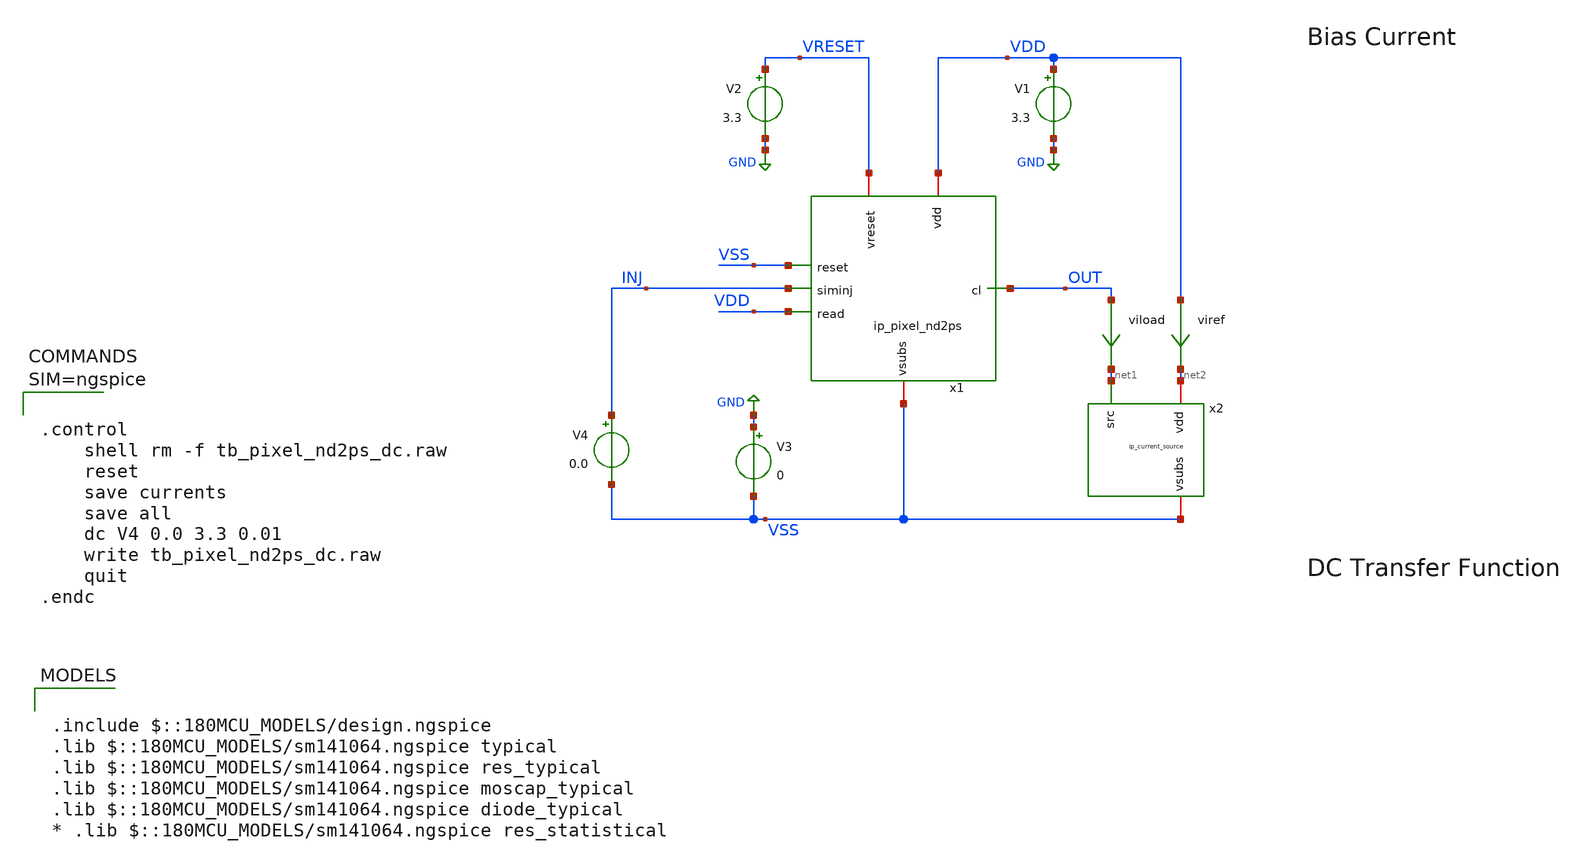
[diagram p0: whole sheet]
** sch_path: xschem/tb_pixel_nd2ps_dc.sch
**.subckt tb_pixel_nd2ps_dc
V1 VDD GND 3.3
V2 VRESET GND 3.3
V3 GND VSS 0
x1 VDD VRESET VSS INJ OUT VDD VSS ip_pixel_nd2ps
V4 INJ VSS 0.0
x2 net2 net1 VSS ip_current_source
viload OUT net1 0
.save i(viload)
viref VDD net2 0
.save i(viref)
**** begin user architecture code

.include $::180MCU_MODELS/design.ngspice
.lib $::180MCU_MODELS/sm141064.ngspice typical
.lib $::180MCU_MODELS/sm141064.ngspice res_typical
.lib $::180MCU_MODELS/sm141064.ngspice moscap_typical
.lib $::180MCU_MODELS/sm141064.ngspice diode_typical
* .lib $::180MCU_MODELS/sm141064.ngspice res_statistical




.control
	shell rm -f tb_pixel_nd2ps_dc.raw
	reset
	save currents
	save all
	dc V4 0.0 3.3 0.01
	write tb_pixel_nd2ps_dc.raw
	quit
.endc



**** end user architecture code
**.ends

* expanding   symbol:  ip_pixel_nd2ps.sym # of pins=7
** sym_path: xschem/ip_pixel_nd2ps.sym
** sch_path: xschem/ip_pixel_nd2ps.sch
.subckt ip_pixel_nd2ps vdd vreset reset siminj cl read vsubs
*.iopin vdd
*.iopin vsubs
*.ipin siminj
*.ipin reset
*.ipin read
*.iopin vreset
*.opin cl
XM1 vreset reset siminj vsubs nfet_03v3 L=0.3u W=0.3u nf=1 ad='int((nf+1)/2) * W/nf * 0.18u' as='int((nf+2)/2) * W/nf * 0.18u'
+ pd='2*int((nf+1)/2) * (W/nf + 0.18u)' ps='2*int((nf+2)/2) * (W/nf + 0.18u)' nrd='0.18u / W' nrs='0.18u / W'
+ sa=0 sb=0 sd=0 m=1
XM2 vdd siminj sfout vsubs nfet_03v3 L=0.3u W=0.3u nf=1 ad='int((nf+1)/2) * W/nf * 0.18u' as='int((nf+2)/2) * W/nf * 0.18u'
+ pd='2*int((nf+1)/2) * (W/nf + 0.18u)' ps='2*int((nf+2)/2) * (W/nf + 0.18u)' nrd='0.18u / W' nrs='0.18u / W'
+ sa=0 sb=0 sd=0 m=1
XM3 sfout read cl vsubs nfet_03v3 L=0.3u W=1u nf=1 ad='int((nf+1)/2) * W/nf * 0.18u' as='int((nf+2)/2) * W/nf * 0.18u'
+ pd='2*int((nf+1)/2) * (W/nf + 0.18u)' ps='2*int((nf+2)/2) * (W/nf + 0.18u)' nrd='0.18u / W' nrs='0.18u / W'
+ sa=0 sb=0 sd=0 m=1
D1 vsubs siminj diode_nd2ps_03v3 area='12u * 10u ' pj='2*12u + 2*10u ' m=1
.ends


* expanding   symbol:  ip_current_source.sym # of pins=3
** sym_path: xschem/ip_current_source.sym
** sch_path: xschem/ip_current_source.sch
.subckt ip_current_source vdd src vsubs
*.iopin vdd
*.iopin vsubs
*.ipin src
XM1 net1 net1 vsubs vsubs nfet_03v3 L=1u W=5u nf=1 ad='int((nf+1)/2) * W/nf * 0.18u' as='int((nf+2)/2) * W/nf * 0.18u'
+ pd='2*int((nf+1)/2) * (W/nf + 0.18u)' ps='2*int((nf+2)/2) * (W/nf + 0.18u)' nrd='0.18u / W' nrs='0.18u / W'
+ sa=0 sb=0 sd=0 m=1
XM2 net2 net1 vsubs vsubs nfet_03v3 L=5u W=0.5u nf=1 ad='int((nf+1)/2) * W/nf * 0.18u' as='int((nf+2)/2) * W/nf * 0.18u'
+ pd='2*int((nf+1)/2) * (W/nf + 0.18u)' ps='2*int((nf+2)/2) * (W/nf + 0.18u)' nrd='0.18u / W' nrs='0.18u / W'
+ sa=0 sb=0 sd=0 m=1
XM3 src net1 net2 vsubs nfet_03v3 L=0.5u W=5u nf=1 ad='int((nf+1)/2) * W/nf * 0.18u' as='int((nf+2)/2) * W/nf * 0.18u'
+ pd='2*int((nf+1)/2) * (W/nf + 0.18u)' ps='2*int((nf+2)/2) * (W/nf + 0.18u)' nrd='0.18u / W' nrs='0.18u / W'
+ sa=0 sb=0 sd=0 m=2
XR1 net1 net4 vsubs ppolyf_u_1k r_width=1e-6 r_length=6e-6 m=1
XR2 net4 net3 vsubs ppolyf_u_1k r_width=1e-6 r_length=6e-6 m=1
XR3 net3 net5 vsubs ppolyf_u_1k r_width=1e-6 r_length=6e-6 m=1
XR4 net5 net7 vsubs ppolyf_u_1k r_width=1e-6 r_length=6e-6 m=1
XR5 net7 net6 vsubs ppolyf_u_1k r_width=1e-6 r_length=6e-6 m=1
XR6 net6 vdd vsubs ppolyf_u_1k r_width=1e-6 r_length=6e-6 m=1
.ends

.GLOBAL GND
.end
